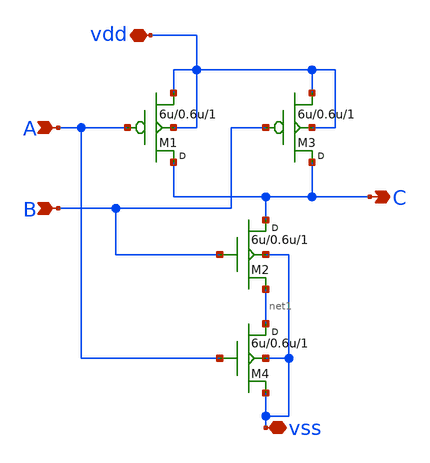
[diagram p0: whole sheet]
** sch_path: lab6/NANDx.sch
**.subckt NANDx vdd A B C vss
*.iopin vdd
*.ipin A
*.ipin B
*.opin C
*.iopin vss
M2 C B net1 vss nfet w=6u l=0.6u m=1
M3 C B vdd vdd pfet w=6u l=0.6u m=1
M1 C A vdd vdd pfet w=6u l=0.6u m=1
M4 net1 A vss vss nfet w=6u l=0.6u m=1
**.ends
.end
